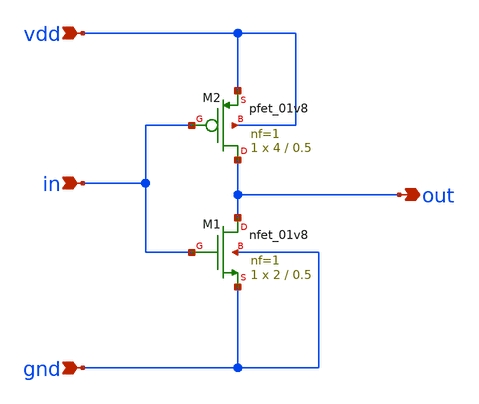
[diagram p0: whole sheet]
** sch_path: xschem/untitled.sch
**.subckt untitled in vdd gnd out
*.ipin in
*.ipin vdd
*.ipin gnd
*.opin out
XM1 out in gnd gnd sky130_fd_pr__nfet_01v8 L=0.5 W=2 nf=1 ad='int((nf+1)/2) * W/nf * 0.29' as='int((nf+2)/2) * W/nf * 0.29'
+ pd='2*int((nf+1)/2) * (W/nf + 0.29)' ps='2*int((nf+2)/2) * (W/nf + 0.29)' nrd='0.29 / W' nrs='0.29 / W'
+ sa=0 sb=0 sd=0 mult=1 m=1
XM2 out in vdd vdd sky130_fd_pr__pfet_01v8 L=0.5 W=4 nf=1 ad='int((nf+1)/2) * W/nf * 0.29' as='int((nf+2)/2) * W/nf * 0.29'
+ pd='2*int((nf+1)/2) * (W/nf + 0.29)' ps='2*int((nf+2)/2) * (W/nf + 0.29)' nrd='0.29 / W' nrs='0.29 / W'
+ sa=0 sb=0 sd=0 mult=1 m=1
**.ends
.end
